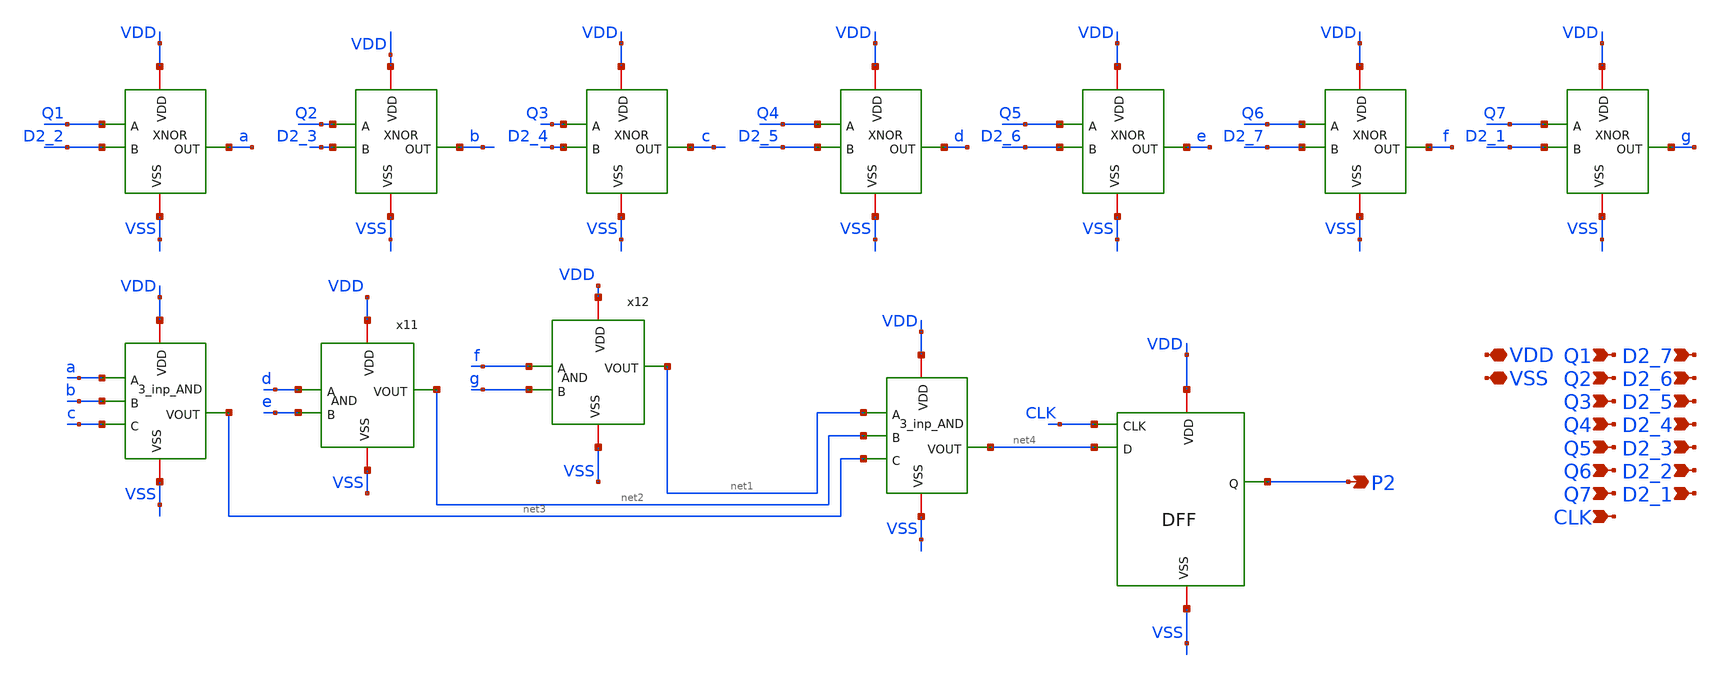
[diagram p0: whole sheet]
** sch_path: Xschem/PLL_TOP_Schematics/P2_GENERATOR.sch
**.subckt P2_GENERATOR VDD VSS Q1 Q2 Q3 Q4 Q5 Q6 Q7 P2 D2_1 D2_2 D2_3 D2_4 D2_5 D2_6 D2_7 CLK
*.iopin VDD
*.iopin VSS
*.ipin Q1
*.ipin Q2
*.ipin Q3
*.ipin Q4
*.ipin Q5
*.ipin Q6
*.ipin Q7
*.opin P2
*.ipin D2_1
*.ipin D2_2
*.ipin D2_3
*.ipin D2_4
*.ipin D2_5
*.ipin D2_6
*.ipin D2_7
*.ipin CLK
x4 VDD Q2 b D2_3 VSS XNOR
x5 VDD Q1 a D2_2 VSS XNOR
x6 VDD Q3 c D2_4 VSS XNOR
x2 VDD Q4 d D2_5 VSS XNOR
x3 VDD Q5 e D2_6 VSS XNOR
x9 VDD Q6 f D2_7 VSS XNOR
x10 VDD Q7 g D2_1 VSS XNOR
x7 VDD net3 a b c VSS 3_inp_AND
x15 VDD net4 net1 net2 net3 VSS 3_inp_AND
x11 VDD net2 d e VSS AND
x12 VDD net1 f g VSS AND
x13 CLK VDD net4 P2 VSS DFF
**.ends
.end
